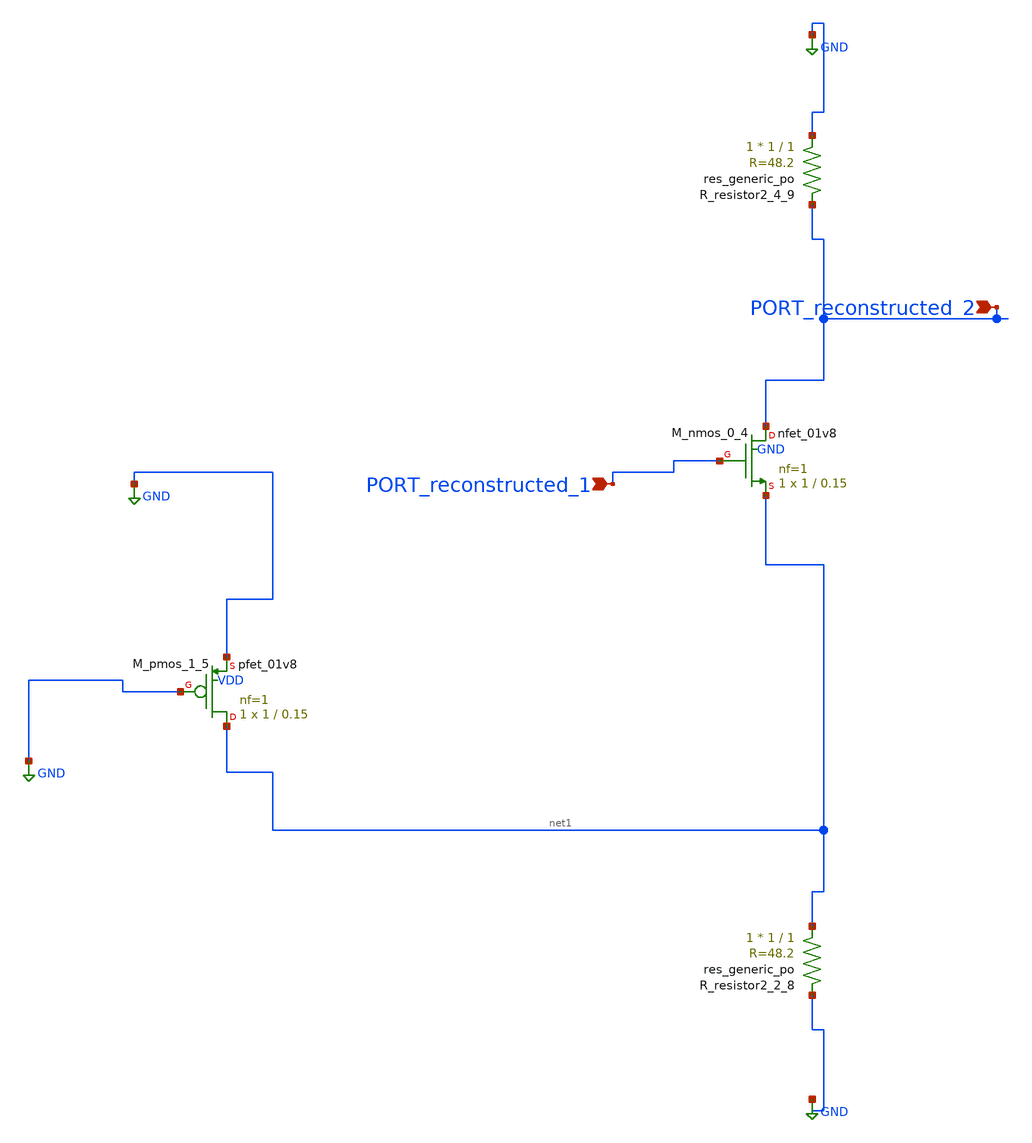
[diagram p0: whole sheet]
** sch_path: schematics/AMSNet/641.sch
**.subckt 641 PORT_reconstructed_1 PORT_reconstructed_2
*.ipin PORT_reconstructed_1
*.ipin PORT_reconstructed_2
XM_nmos_0_4 PORT_reconstructed_2 PORT_reconstructed_1 net1 GND sky130_fd_pr__nfet_01v8 L=0.15 W=1 nf=1
+ ad='int((1 + 1)/2) * 1 / 1 * 0.29' as='int((1 + 2)/2) * 1 / 1 * 0.29' pd='2*int((1 + 1)/2) * (1 / 1 + 0.29)'
+ ps='2*int((1 + 2)/2) * (1 / 1 + 0.29)' nrd='0.29 / 1 ' nrs='0.29 / 1 ' sa=0 sb=0 sd=0 mult=1 m=1
XM_pmos_1_5 net1 GND GND VDD sky130_fd_pr__pfet_01v8 L=0.15 W=1 nf=1 ad='int((1 + 1)/2) * 1 / 1 * 0.29'
+ as='int((1 + 2)/2) * 1 / 1 * 0.29' pd='2*int((1 + 1)/2) * (1 / 1 + 0.29)' ps='2*int((1 + 2)/2) * (1 / 1 + 0.29)'
+ nrd='0.29 / 1 ' nrs='0.29 / 1 ' sa=0 sb=0 sd=0 mult=1 m=1
XR_resistor2_2_8 net1 GND sky130_fd_pr__res_generic_po W=1 L=1 m=1
XR_resistor2_4_9 GND PORT_reconstructed_2 sky130_fd_pr__res_generic_po W=1 L=1 m=1
**.ends
.GLOBAL GND
.end
